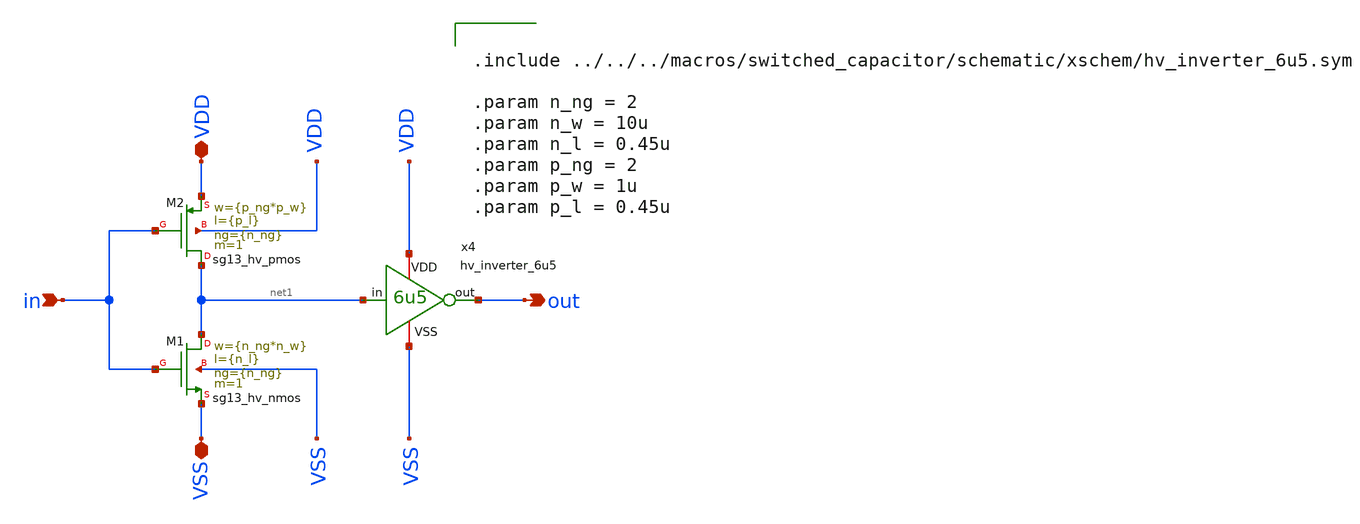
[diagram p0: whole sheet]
** sch_path: macros/heichips26_vcr/macros/switched_capacitor/schematic/xschem/lvl_shift_up.sch
**.subckt lvl_shift_up in VDD VSS out
*.ipin in
*.iopin VDD
*.iopin VSS
*.opin out
XM1 net1 in VSS VSS sg13_hv_nmos w={n_ng*n_w} l={n_l} ng={n_ng} m=1 mm_ok=1
XM2 net1 in VDD VDD sg13_hv_pmos w={p_ng*p_w} l={p_l} ng={n_ng} m=1 mm_ok=1
x4 VDD net1 out VSS hv_inverter_6u5
**** begin user architecture code


.include ../../../macros/switched_capacitor/schematic/xschem/hv_inverter_6u5.sym

.param n_ng = 2
.param n_w = 10u
.param n_l = 0.45u
.param p_ng = 2
.param p_w = 1u
.param p_l = 0.45u


**** end user architecture code
**.ends

* expanding   symbol:  hv_inverter_6u5.sym # of pins=4
** sym_path: macros/heichips26_vcr/macros/switched_capacitor/schematic/xschem/hv_inverter_6u5.sym
** sch_path: macros/heichips26_vcr/macros/switched_capacitor/schematic/xschem/hv_inverter_6u5.sch
.subckt hv_inverter_6u5 VDD in out VSS
*.ipin in
*.iopin VDD
*.iopin VSS
*.opin out
XM2 out in VSS VSS sg13_hv_nmos w={n_w} l={n_l} ng={ng} m=1 mm_ok=1
XM3 out in VDD VDD sg13_hv_pmos w={p_w} l={p_l} ng={ng} m=1 mm_ok=1
**** begin user architecture code


.param ng  = 1
.param n_ng = ng
.param n_w = {2u*n_ng}
.param n_l = 0.45u
.param p_ng = ng
.param p_w = {6.5u*p_ng}
.param p_l = 0.4u


**** end user architecture code
.ends

.end
